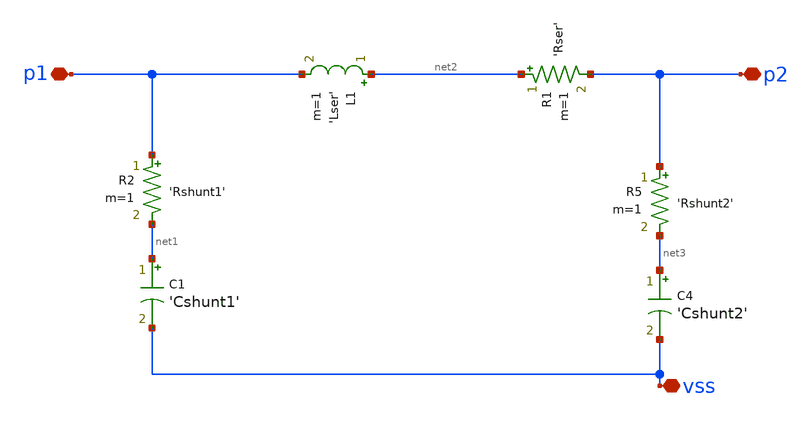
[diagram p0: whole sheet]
** sch_path: LNA7096-main/schematic/xschem/01_lna/ind_rlc.sch
**.subckt ind_rlc p1 p2 vss
*.iopin p1
*.iopin p2
*.iopin vss
L1 net2 p1 'Lser' m=1
R1 net2 p2 'Rser' m=1
R2 p1 net1 'Rshunt1' m=1
C1 net1 vss 'Cshunt1' m=1
R5 p2 net3 'Rshunt2' m=1
C4 net3 vss 'Cshunt2' m=1
**.ends
.end
